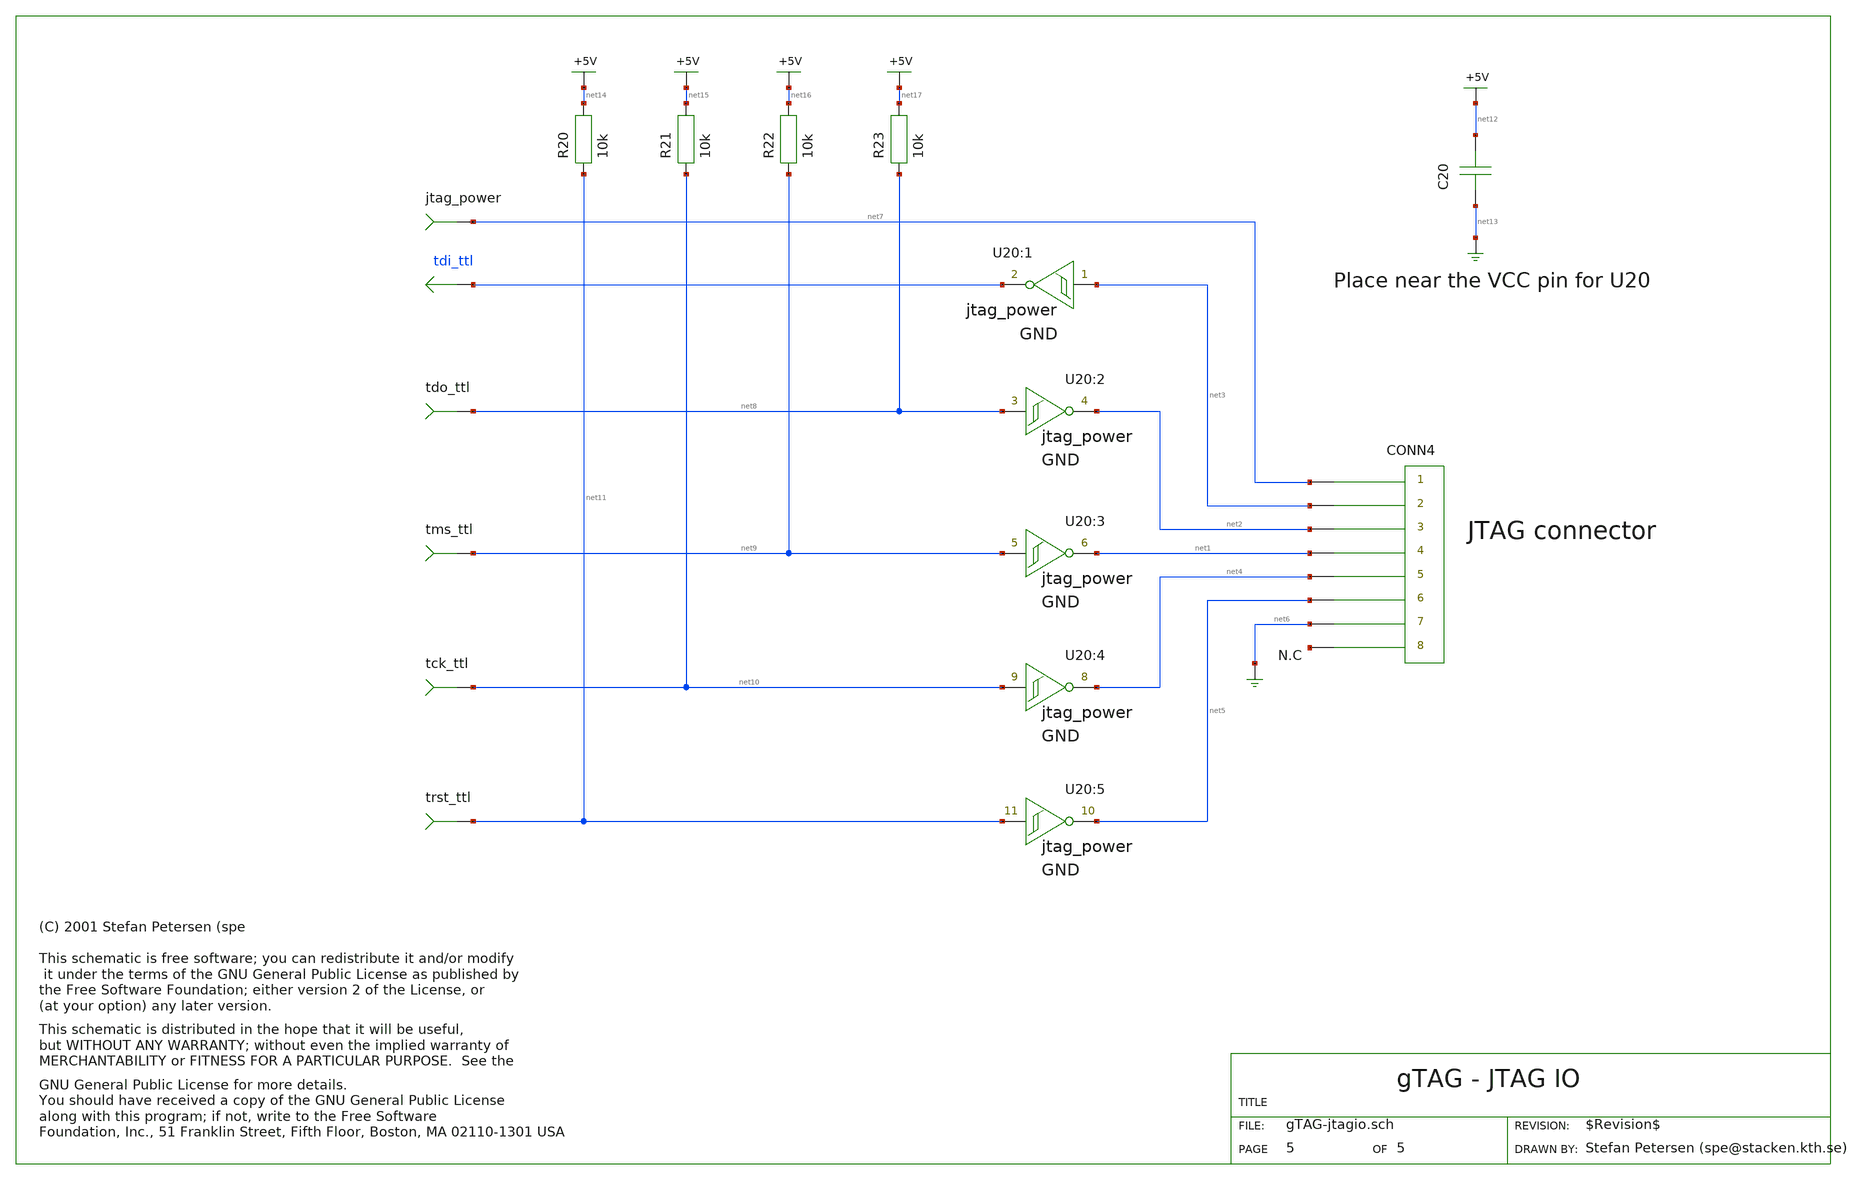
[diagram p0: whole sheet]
** sch_path: xschem_library/gschem_import/gTAG-jtagio.sch
* copyleft.sym
**.subckt gTAG-jtagio tdi_ttl
tdo_ttl net8
tms_ttl net9
tck_ttl net10
trst_ttl net11
jtag_power net7
U20:1 net3 tdi_ttl Vcc GND
U20:2 net8 net2 Vcc GND
U20:3 net9 net1 Vcc GND
U20:4 net10 net4 Vcc GND
U20:5 net11 net5 Vcc GND
CONN4 net7 net3 net2 net1 net4 net5 net6 net18
CONN4
C20 net13 net12 100n
C20 net12
R20 net11 net14 10k
R21 net10 net15 10k
R22 net9 net16 10k
R23 net8 net17 10k
R23 net14
R23 net15
R23 net16
R23 net17
**.ends
.end
